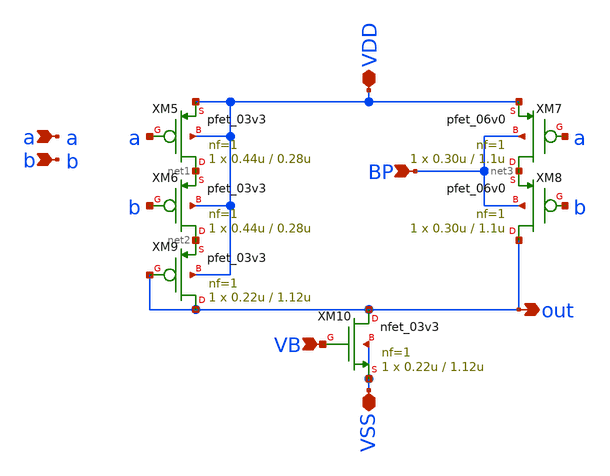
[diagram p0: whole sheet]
** sch_path: xschem_sn2/NMAX.sch
**.subckt NMAX VSS VB BP VDD out a b
*.iopin VSS
*.ipin VB
*.ipin BP
*.iopin VDD
*.opin out
*.ipin a
*.ipin b
XM5 net1 a VDD VDD pfet_03v3 L=0.28u W=0.44u nf=1 ad='int((nf+1)/2) * W/nf * 0.18u' as='int((nf+2)/2) * W/nf * 0.18u'
+ pd='2*int((nf+1)/2) * (W/nf + 0.18u)' ps='2*int((nf+2)/2) * (W/nf + 0.18u)' nrd='0.18u / W' nrs='0.18u / W'
+ sa=0 sb=0 sd=0 m=1 par=1
XM6 net2 b net1 VDD pfet_03v3 L=0.28u W=0.44u nf=1 ad='int((nf+1)/2) * W/nf * 0.18u' as='int((nf+2)/2) * W/nf * 0.18u'
+ pd='2*int((nf+1)/2) * (W/nf + 0.18u)' ps='2*int((nf+2)/2) * (W/nf + 0.18u)' nrd='0.18u / W' nrs='0.18u / W'
+ sa=0 sb=0 sd=0 m=1 par=1
XM7 net3 a VDD BP pfet_06v0 L=1.1u W=0.30u nf=1 ad='int((nf+1)/2) * W/nf * 0.18u' as='int((nf+2)/2) * W/nf * 0.18u'
+ pd='2*int((nf+1)/2) * (W/nf + 0.18u)' ps='2*int((nf+2)/2) * (W/nf + 0.18u)' nrd='0.18u / W' nrs='0.18u / W'
+ sa=0 sb=0 sd=0 m=1
XM8 out b net3 BP pfet_06v0 L=1.1u W=0.30u nf=1 ad='int((nf+1)/2) * W/nf * 0.18u' as='int((nf+2)/2) * W/nf * 0.18u'
+ pd='2*int((nf+1)/2) * (W/nf + 0.18u)' ps='2*int((nf+2)/2) * (W/nf + 0.18u)' nrd='0.18u / W' nrs='0.18u / W'
+ sa=0 sb=0 sd=0 m=1
XM9 out out net2 VDD pfet_03v3 L=1.12u W=0.22u nf=1 ad='int((nf+1)/2) * W/nf * 0.18u' as='int((nf+2)/2) * W/nf * 0.18u'
+ pd='2*int((nf+1)/2) * (W/nf + 0.18u)' ps='2*int((nf+2)/2) * (W/nf + 0.18u)' nrd='0.18u / W' nrs='0.18u / W'
+ sa=0 sb=0 sd=0 m=1 par=1
XM10 out VB VSS VSS nfet_03v3 L=1.12u W=0.22u nf=1 ad='int((nf+1)/2) * W/nf * 0.18u' as='int((nf+2)/2) * W/nf * 0.18u'
+ pd='2*int((nf+1)/2) * (W/nf + 0.18u)' ps='2*int((nf+2)/2) * (W/nf + 0.18u)' nrd='0.18u / W' nrs='0.18u / W'
+ sa=0 sb=0 sd=0 m=1 par=1
**.ends
.end
